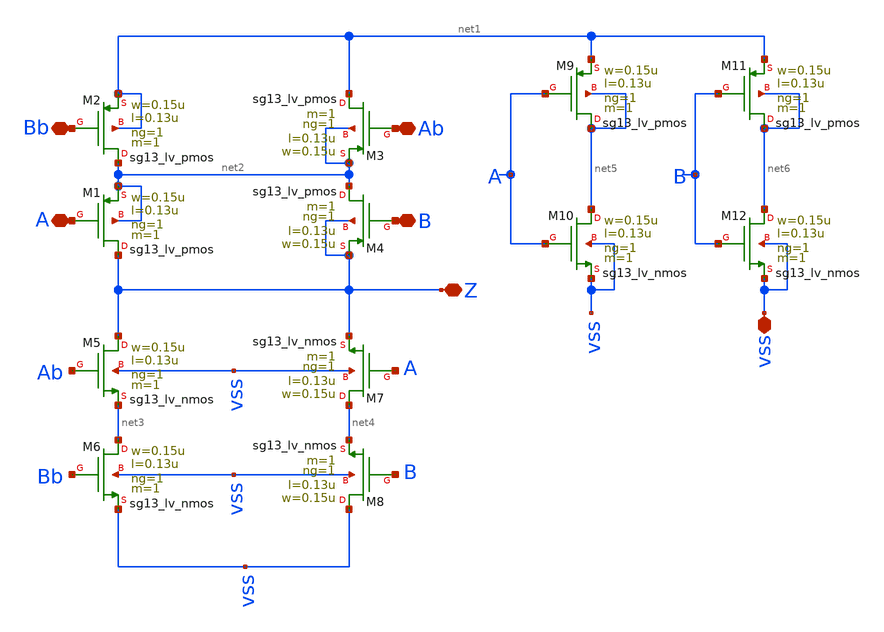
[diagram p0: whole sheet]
** sch_path: design/blocks/puertaxor/puertaxor.sch
**.subckt puertaxor A Bb Ab B vss Z
*.iopin A
*.iopin Bb
*.iopin Ab
*.iopin B
*.iopin vss
*.iopin Z
XM1 Z A net2 net2 sg13_lv_pmos w=0.15u l=0.13u ng=1 m=1 mm_ok=1
XM2 net2 Bb net1 net1 sg13_lv_pmos w=0.15u l=0.13u ng=1 m=1 mm_ok=1
XM3 net1 Ab net2 net2 sg13_lv_pmos w=0.15u l=0.13u ng=1 m=1 mm_ok=1
XM4 net2 B Z Z sg13_lv_pmos w=0.15u l=0.13u ng=1 m=1 mm_ok=1
XM5 Z Ab net3 vss sg13_lv_nmos w=0.15u l=0.13u ng=1 m=1 mm_ok=1
XM6 net3 Bb vss vss sg13_lv_nmos w=0.15u l=0.13u ng=1 m=1 mm_ok=1
XM7 net4 A Z vss sg13_lv_nmos w=0.15u l=0.13u ng=1 m=1 mm_ok=1
XM8 vss B net4 vss sg13_lv_nmos w=0.15u l=0.13u ng=1 m=1 mm_ok=1
XM9 net5 A net1 net5 sg13_lv_pmos w=0.15u l=0.13u ng=1 m=1 mm_ok=1
XM10 net5 A vss vss sg13_lv_nmos w=0.15u l=0.13u ng=1 m=1 mm_ok=1
XM11 net6 B net1 net6 sg13_lv_pmos w=0.15u l=0.13u ng=1 m=1 mm_ok=1
XM12 net6 B vss vss sg13_lv_nmos w=0.15u l=0.13u ng=1 m=1 mm_ok=1
**.ends
.end
